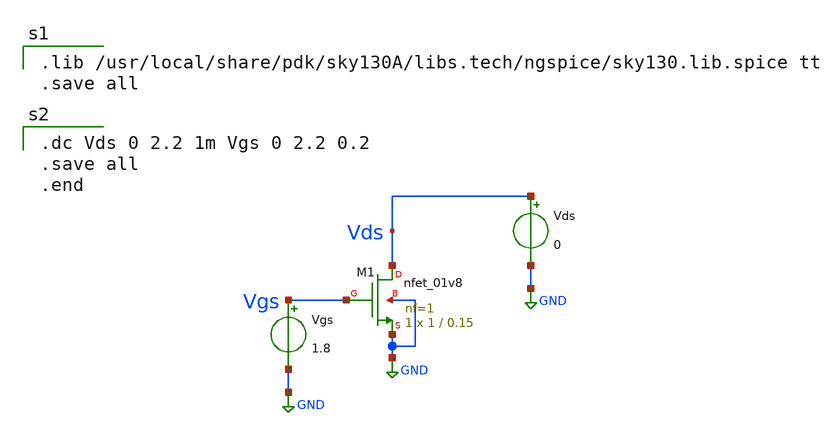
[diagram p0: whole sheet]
** sch_path: OneDrive/Documents/CMOS-Inverter-Design-and-Analysis-using-Sky130pdk-main/xschem/nmos_01v8.sch
**.subckt nmos_01v8
XM1 Vds Vgs GND GND sky130_fd_pr__nfet_01v8 L=0.15 W=1 nf=1 ad='int((1 + 1)/2) * 1 / 1 * 0.29' as='int((1 + 2)/2) * 1 / 1 * 0.29'
+ pd='2*int((1 + 1)/2) * (1 / 1 + 0.29)' ps='2*int((1 + 2)/2) * (1 / 1 + 0.29)' nrd='0.29 / 1 ' nrs='0.29 / 1 '
+ sa=0 sb=0 sd=0 mult=1 m=1
Vgs Vgs GND 1.8
Vds Vds GND 0
**** begin user architecture code

.lib /usr/local/share/pdk/sky130A/libs.tech/ngspice/sky130.lib.spice tt
.save all


.dc Vds 0 2.2 1m Vgs 0 2.2 0.2
.save all
.end

**** end user architecture code
**.ends
.GLOBAL GND
.end
